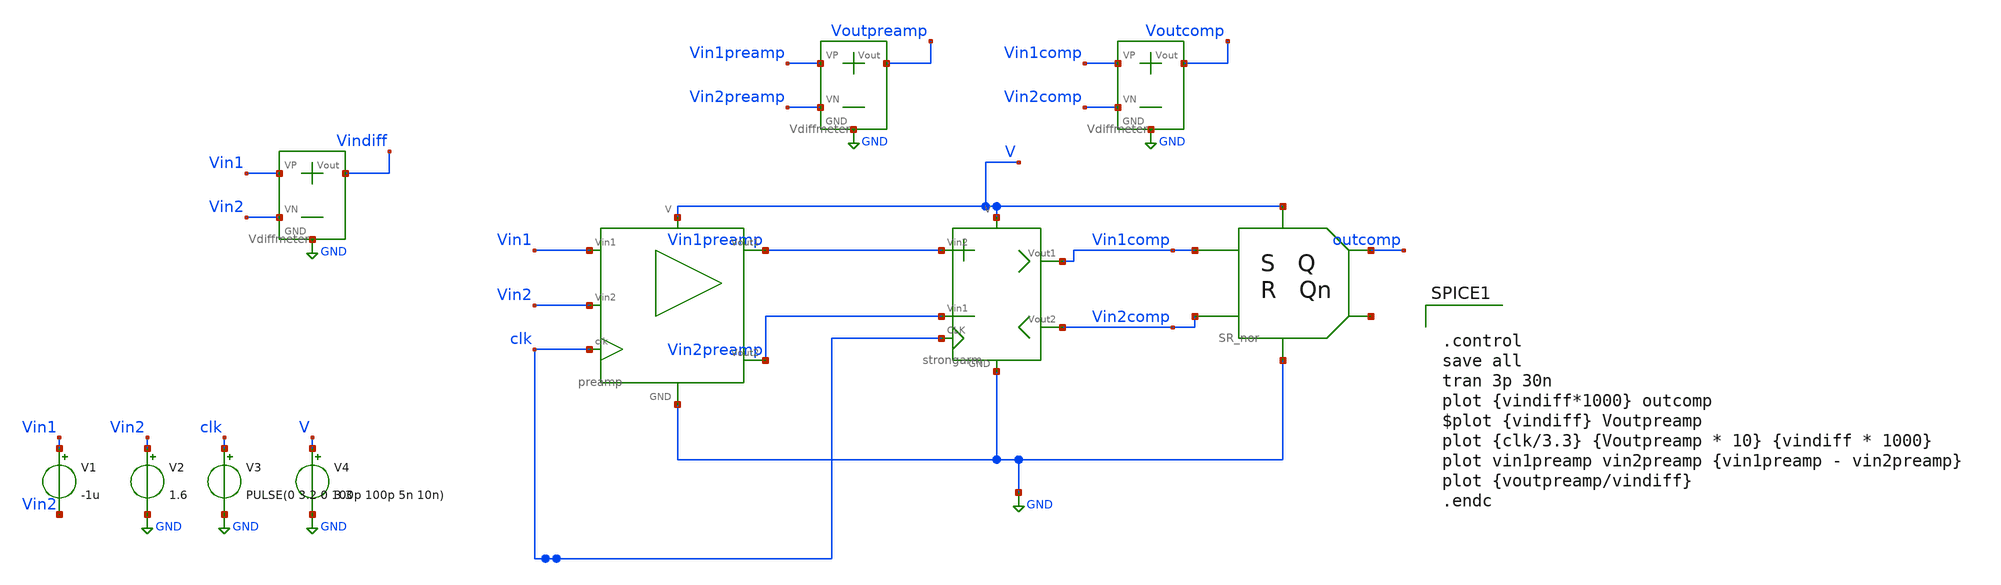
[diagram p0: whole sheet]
** sch_path: SAR_ADC/xschem/test/comp_full_tb/no_symbol/dc__tb.sch
**.subckt dc__tb
V1 Vin1 Vin2 -1u
V2 Vin2 GND 1.6
V3 clk GND PULSE(0 3.2 0 100p 100p 5n 10n)
V4 V GND 3.3
X2 Vin1preamp Vin2preamp Voutpreamp GND Vdiffmeter
X6 Vin1comp Vin2comp Voutcomp GND Vdiffmeter
X5 Vin1 Vin2 Vindiff GND Vdiffmeter
X3 V GND Vin1 clk Vin1preamp Vin2preamp Vin2 preamp
X4 V GND Vin2preamp Vin1preamp clk Vin1comp Vin2comp strongarm
X1 Vin1comp V GND Vin2comp outcomp net1 SR_nor
**** begin user architecture code


.control
save all
tran 3p 30n
plot {vindiff*1000} outcomp
$plot {vindiff} Voutpreamp
plot {clk/3.3} {Voutpreamp * 10} {vindiff * 1000}
plot vin1preamp vin2preamp {vin1preamp - vin2preamp}
plot {voutpreamp/vindiff}
.endc


.include $env(PDK_ROOT)/$env(PDK)/libs.tech/ngspice/design.ngspice
.lib $env(PDK_ROOT)/$env(PDK)/libs.tech/ngspice/sm141064.ngspice typical

**** end user architecture code
**.ends

* expanding   symbol:  ../../../../symbols/Vdiffmeter.sym # of pins=4
** sym_path: SAR_ADC/xschem/spice/symbols/Vdiffmeter.sym
** sch_path: SAR_ADC/xschem/spice/symbols/Vdiffmeter.sch
.subckt Vdiffmeter VP VN Vout GND
*.iopin Vout
*.iopin GND
*.iopin VP
*.iopin VN
R4 Vout GND 1k m=1
E4 Vout GND VP VN 1
.ends


* expanding   symbol:  ../../../../symbols/preamp.sym # of pins=7
** sym_path: SAR_ADC/xschem/designs/preamp.sym
** sch_path: SAR_ADC/xschem/designs/preamp.sch
.subckt preamp V GND Vin1 clk Vout1 Vout2 Vin2
*.iopin V
*.iopin GND
*.iopin Vout2
*.iopin Vout1
*.iopin clk
*.iopin Vin2
*.iopin Vin1
XM26 Vout2 clk GND GND nfet_03v3 L=.5u W=.22u nf=1 ad='int((nf+1)/2) * W/nf * 0.18u' as='int((nf+2)/2) * W/nf * 0.18u'
+ pd='2*int((nf+1)/2) * (W/nf + 0.18u)' ps='2*int((nf+2)/2) * (W/nf + 0.18u)' nrd='0.18u / W' nrs='0.18u / W'
+ sa=0 sb=0 sd=0 m=1
XM27 Vout1 clk GND GND nfet_03v3 L=.5u W=.22u nf=1 ad='int((nf+1)/2) * W/nf * 0.18u' as='int((nf+2)/2) * W/nf * 0.18u'
+ pd='2*int((nf+1)/2) * (W/nf + 0.18u)' ps='2*int((nf+2)/2) * (W/nf + 0.18u)' nrd='0.18u / W' nrs='0.18u / W'
+ sa=0 sb=0 sd=0 m=1
XM24 Vout1 Vin2 net1 V pfet_03v3 L=.28u W=8u nf=1 ad='int((nf+1)/2) * W/nf * 0.18u' as='int((nf+2)/2) * W/nf * 0.18u'
+ pd='2*int((nf+1)/2) * (W/nf + 0.18u)' ps='2*int((nf+2)/2) * (W/nf + 0.18u)' nrd='0.18u / W' nrs='0.18u / W'
+ sa=0 sb=0 sd=0 m=1
XM25 Vout2 Vin1 net1 V pfet_03v3 L=.28u W=8u nf=1 ad='int((nf+1)/2) * W/nf * 0.18u' as='int((nf+2)/2) * W/nf * 0.18u'
+ pd='2*int((nf+1)/2) * (W/nf + 0.18u)' ps='2*int((nf+2)/2) * (W/nf + 0.18u)' nrd='0.18u / W' nrs='0.18u / W'
+ sa=0 sb=0 sd=0 m=1
XM1 V clk net1 V pfet_03v3 L=2u W=1u nf=1 ad='int((nf+1)/2) * W/nf * 0.18u' as='int((nf+2)/2) * W/nf * 0.18u'
+ pd='2*int((nf+1)/2) * (W/nf + 0.18u)' ps='2*int((nf+2)/2) * (W/nf + 0.18u)' nrd='0.18u / W' nrs='0.18u / W'
+ sa=0 sb=0 sd=0 m=1
.ends


* expanding   symbol:  ../../../../symbols/strongarm.sym # of pins=7
** sym_path: SAR_ADC/xschem/designs/strongarm.sym
** sch_path: SAR_ADC/xschem/designs/strongarm.sch
.subckt strongarm V GND Vin1 Vin2 CLK Vout1 Vout2
*.iopin V
*.iopin Vout1
*.iopin Vin1
*.iopin Vin2
*.iopin Vout2
*.iopin CLK
*.iopin GND
XM1 net3 Vout2 V V pfet_03v3 L=0.28u W=2u nf=1 ad='int((nf+1)/2) * W/nf * 0.18u' as='int((nf+2)/2) * W/nf * 0.18u'
+ pd='2*int((nf+1)/2) * (W/nf + 0.18u)' ps='2*int((nf+2)/2) * (W/nf + 0.18u)' nrd='0.18u / W' nrs='0.18u / W'
+ sa=0 sb=0 sd=0 m=1
XM2 Vout1 net1 GND GND nfet_03v3 L=0.28u W=2u nf=1 ad='int((nf+1)/2) * W/nf * 0.18u' as='int((nf+2)/2) * W/nf * 0.18u'
+ pd='2*int((nf+1)/2) * (W/nf + 0.18u)' ps='2*int((nf+2)/2) * (W/nf + 0.18u)' nrd='0.18u / W' nrs='0.18u / W'
+ sa=0 sb=0 sd=0 m=1
XM3 Vout2 Vout1 GND GND nfet_03v3 L=0.28u W=2u nf=1 ad='int((nf+1)/2) * W/nf * 0.18u' as='int((nf+2)/2) * W/nf * 0.18u'
+ pd='2*int((nf+1)/2) * (W/nf + 0.18u)' ps='2*int((nf+2)/2) * (W/nf + 0.18u)' nrd='0.18u / W' nrs='0.18u / W'
+ sa=0 sb=0 sd=0 m=1
XM4 Vout2 net1 GND GND nfet_03v3 L=0.28u W=2u nf=1 ad='int((nf+1)/2) * W/nf * 0.18u' as='int((nf+2)/2) * W/nf * 0.18u'
+ pd='2*int((nf+1)/2) * (W/nf + 0.18u)' ps='2*int((nf+2)/2) * (W/nf + 0.18u)' nrd='0.18u / W' nrs='0.18u / W'
+ sa=0 sb=0 sd=0 m=1
XM5 Vout1 Vout2 GND GND nfet_03v3 L=0.28u W=2u nf=1 ad='int((nf+1)/2) * W/nf * 0.18u' as='int((nf+2)/2) * W/nf * 0.18u'
+ pd='2*int((nf+1)/2) * (W/nf + 0.18u)' ps='2*int((nf+2)/2) * (W/nf + 0.18u)' nrd='0.18u / W' nrs='0.18u / W'
+ sa=0 sb=0 sd=0 m=1
XM6 net2 Vout1 V V pfet_03v3 L=0.28u W=2u nf=1 ad='int((nf+1)/2) * W/nf * 0.18u' as='int((nf+2)/2) * W/nf * 0.18u'
+ pd='2*int((nf+1)/2) * (W/nf + 0.18u)' ps='2*int((nf+2)/2) * (W/nf + 0.18u)' nrd='0.18u / W' nrs='0.18u / W'
+ sa=0 sb=0 sd=0 m=1
XM7 Vout1 Vin1 net3 V pfet_03v3 L=0.28u W=10u nf=1 ad='int((nf+1)/2) * W/nf * 0.18u' as='int((nf+2)/2) * W/nf * 0.18u'
+ pd='2*int((nf+1)/2) * (W/nf + 0.18u)' ps='2*int((nf+2)/2) * (W/nf + 0.18u)' nrd='0.18u / W' nrs='0.18u / W'
+ sa=0 sb=0 sd=0 m=1
XM8 Vout2 Vin2 net2 V pfet_03v3 L=0.28u W=10u nf=1 ad='int((nf+1)/2) * W/nf * 0.18u' as='int((nf+2)/2) * W/nf * 0.18u'
+ pd='2*int((nf+1)/2) * (W/nf + 0.18u)' ps='2*int((nf+2)/2) * (W/nf + 0.18u)' nrd='0.18u / W' nrs='0.18u / W'
+ sa=0 sb=0 sd=0 m=1
x1 V GND net4 CLK inv cl=0.28u wp=0.44u wn=0.22u wx=4u
x2 V GND net1 net4 inv cl=0.28u wp=0.44u wn=0.22u wx=4u
.ends


* expanding   symbol:  ../../../../symbols/SR_nor.sym # of pins=6
** sym_path: SAR_ADC/xschem/designs/SR_nor.sym
** sch_path: SAR_ADC/xschem/designs/SR_nor.sch
.subckt SR_nor S V GND R Q Qn
*.iopin V
*.iopin GND
*.iopin S
*.iopin R
*.iopin Qn
*.iopin Q
X1 S Q Qn GND V norgate
X2 Qn R Q GND V norgate
.ends


* expanding   symbol:  inv.sym # of pins=4
** sym_path: SAR_ADC/xschem/designs/inv.sym
** sch_path: SAR_ADC/xschem/designs/inv.sch
.subckt inv vdd gnd vout vin  cl=0.28u wp=0.44u wn=0.22u wx=0.22u
*.ipin gnd
*.ipin vdd
*.ipin vin
*.opin vout
XM1 gnd vin vout gnd nfet_03v3 L=0.28u W=8u nf=1 ad='int((nf+1)/2) * W/nf * 0.18u' as='int((nf+2)/2) * W/nf * 0.18u'
+ pd='2*int((nf+1)/2) * (W/nf + 0.18u)' ps='2*int((nf+2)/2) * (W/nf + 0.18u)' nrd='0.18u / W' nrs='0.18u / W'
+ sa=0 sb=0 sd=0 m=1
XM2 vdd vin vout vdd pfet_03v3 L=0.28u W=8u nf=1 ad='int((nf+1)/2) * W/nf * 0.18u' as='int((nf+2)/2) * W/nf * 0.18u'
+ pd='2*int((nf+1)/2) * (W/nf + 0.18u)' ps='2*int((nf+2)/2) * (W/nf + 0.18u)' nrd='0.18u / W' nrs='0.18u / W'
+ sa=0 sb=0 sd=0 m=1
.ends


* expanding   symbol:  norgate.sym # of pins=5
** sym_path: SAR_ADC/xschem/designs/norgate.sym
** sch_path: SAR_ADC/xschem/designs/norgate.sch
.subckt norgate A B Z GND V
*.iopin GND
*.iopin A
*.iopin B
*.iopin V
*.iopin Z
XM3 V A net2 V pfet_03v3 L=0.28u W=0.22u nf=1 ad='int((nf+1)/2) * W/nf * 0.18u' as='int((nf+2)/2) * W/nf * 0.18u'
+ pd='2*int((nf+1)/2) * (W/nf + 0.18u)' ps='2*int((nf+2)/2) * (W/nf + 0.18u)' nrd='0.18u / W' nrs='0.18u / W'
+ sa=0 sb=0 sd=0 m=1
XM6 net2 B Z V pfet_03v3 L=0.28u W=0.22u nf=1 ad='int((nf+1)/2) * W/nf * 0.18u' as='int((nf+2)/2) * W/nf * 0.18u'
+ pd='2*int((nf+1)/2) * (W/nf + 0.18u)' ps='2*int((nf+2)/2) * (W/nf + 0.18u)' nrd='0.18u / W' nrs='0.18u / W'
+ sa=0 sb=0 sd=0 m=1
XM9 V B net1 V pfet_03v3 L=0.28u W=0.22u nf=1 ad='int((nf+1)/2) * W/nf * 0.18u' as='int((nf+2)/2) * W/nf * 0.18u'
+ pd='2*int((nf+1)/2) * (W/nf + 0.18u)' ps='2*int((nf+2)/2) * (W/nf + 0.18u)' nrd='0.18u / W' nrs='0.18u / W'
+ sa=0 sb=0 sd=0 m=1
XM12 net1 A Z V pfet_03v3 L=0.28u W=0.22u nf=1 ad='int((nf+1)/2) * W/nf * 0.18u' as='int((nf+2)/2) * W/nf * 0.18u'
+ pd='2*int((nf+1)/2) * (W/nf + 0.18u)' ps='2*int((nf+2)/2) * (W/nf + 0.18u)' nrd='0.18u / W' nrs='0.18u / W'
+ sa=0 sb=0 sd=0 m=1
XM2 Z B GND GND nfet_03v3 L=0.28u W=0.22u nf=1 ad='int((nf+1)/2) * W/nf * 0.18u' as='int((nf+2)/2) * W/nf * 0.18u'
+ pd='2*int((nf+1)/2) * (W/nf + 0.18u)' ps='2*int((nf+2)/2) * (W/nf + 0.18u)' nrd='0.18u / W' nrs='0.18u / W'
+ sa=0 sb=0 sd=0 m=1
XM4 Z A GND GND nfet_03v3 L=0.28u W=0.22u nf=1 ad='int((nf+1)/2) * W/nf * 0.18u' as='int((nf+2)/2) * W/nf * 0.18u'
+ pd='2*int((nf+1)/2) * (W/nf + 0.18u)' ps='2*int((nf+2)/2) * (W/nf + 0.18u)' nrd='0.18u / W' nrs='0.18u / W'
+ sa=0 sb=0 sd=0 m=1
.ends

.GLOBAL GND
.end
